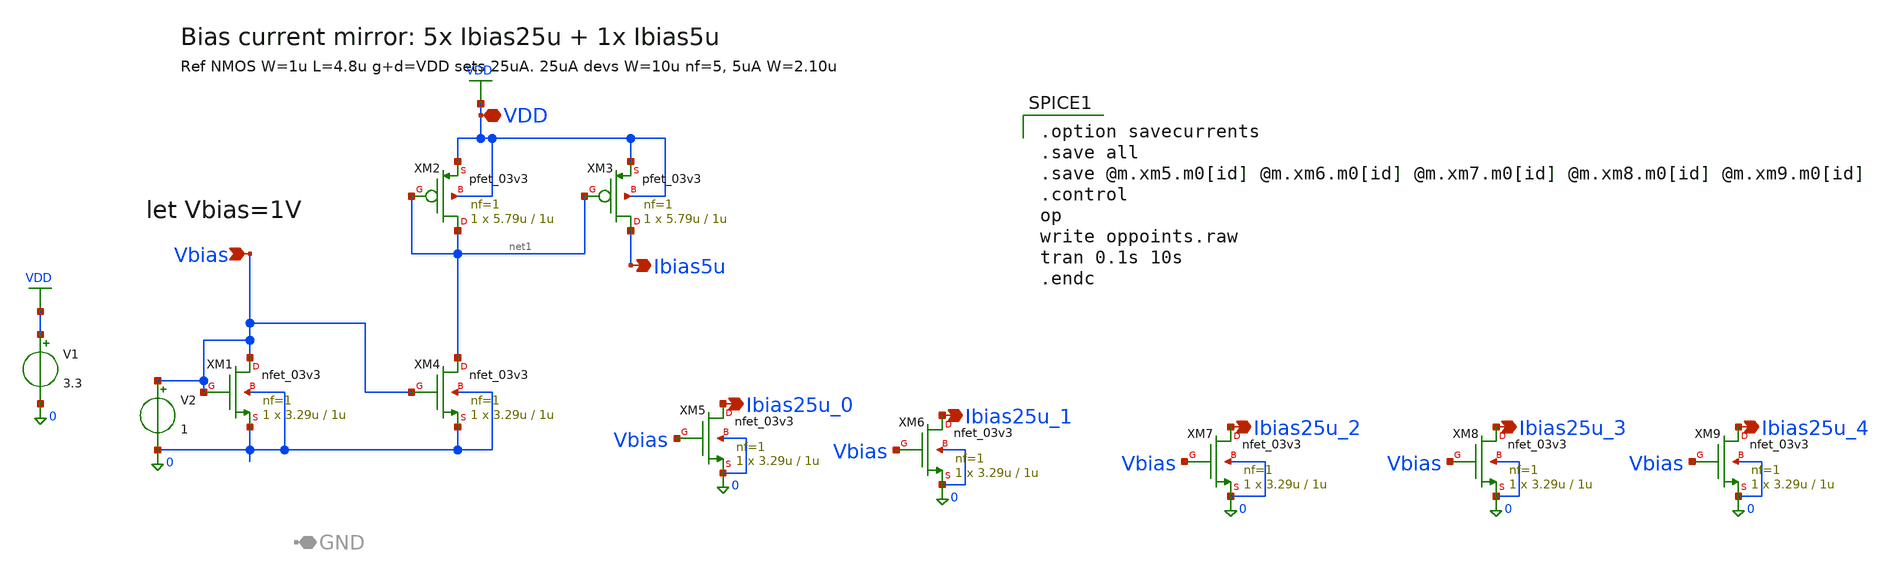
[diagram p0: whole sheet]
** sch_path: ps-bias/jz_bias_tb.sch
**.subckt jz_bias_tb Ibias25u_0 Ibias25u_1 Ibias25u_2 Ibias25u_3 Ibias25u_4 Ibias5u VDD Vbias
*.opin Ibias25u_0
*.opin Ibias25u_1
*.opin Ibias25u_2
*.opin Ibias25u_3
*.opin Ibias25u_4
*.opin Ibias5u
*.iopin VDD
*.ipin Vbias
XM2 net1 net1 VDD VDD pfet_03v3 L=1u W=5.79u nf=1 ad='int((nf+1)/2) * W/nf * 0.18u' as='int((nf+2)/2) * W/nf * 0.18u'
+ pd='2*int((nf+1)/2) * (W/nf + 0.18u)' ps='2*int((nf+2)/2) * (W/nf + 0.18u)' nrd='0.18u / W' nrs='0.18u / W'
+ sa=0 sb=0 sd=0 m=1
XM3 Ibias5u net1 VDD VDD pfet_03v3 L=1u W=5.79u nf=1 ad='int((nf+1)/2) * W/nf * 0.18u' as='int((nf+2)/2) * W/nf * 0.18u'
+ pd='2*int((nf+1)/2) * (W/nf + 0.18u)' ps='2*int((nf+2)/2) * (W/nf + 0.18u)' nrd='0.18u / W' nrs='0.18u / W'
+ sa=0 sb=0 sd=0 m=1
V1 VDD 0 3.3
V2 Vbias 0 1
XM1 Vbias Vbias 0 0 nfet_03v3 L=1u W=3.29u nf=1 ad='int((nf+1)/2) * W/nf * 0.18u' as='int((nf+2)/2) * W/nf * 0.18u'
+ pd='2*int((nf+1)/2) * (W/nf + 0.18u)' ps='2*int((nf+2)/2) * (W/nf + 0.18u)' nrd='0.18u / W' nrs='0.18u / W'
+ sa=0 sb=0 sd=0 m=1
XM4 net1 Vbias 0 0 nfet_03v3 L=1u W=3.29u nf=1 ad='int((nf+1)/2) * W/nf * 0.18u' as='int((nf+2)/2) * W/nf * 0.18u'
+ pd='2*int((nf+1)/2) * (W/nf + 0.18u)' ps='2*int((nf+2)/2) * (W/nf + 0.18u)' nrd='0.18u / W' nrs='0.18u / W'
+ sa=0 sb=0 sd=0 m=1
XM5 Ibias25u_0 Vbias 0 0 nfet_03v3 L=1u W=3.29u nf=1 ad='int((nf+1)/2) * W/nf * 0.18u' as='int((nf+2)/2) * W/nf * 0.18u'
+ pd='2*int((nf+1)/2) * (W/nf + 0.18u)' ps='2*int((nf+2)/2) * (W/nf + 0.18u)' nrd='0.18u / W' nrs='0.18u / W'
+ sa=0 sb=0 sd=0 m=1
XM6 Ibias25u_1 Vbias 0 0 nfet_03v3 L=1u W=3.29u nf=1 ad='int((nf+1)/2) * W/nf * 0.18u' as='int((nf+2)/2) * W/nf * 0.18u'
+ pd='2*int((nf+1)/2) * (W/nf + 0.18u)' ps='2*int((nf+2)/2) * (W/nf + 0.18u)' nrd='0.18u / W' nrs='0.18u / W'
+ sa=0 sb=0 sd=0 m=1
XM7 Ibias25u_2 Vbias 0 0 nfet_03v3 L=1u W=3.29u nf=1 ad='int((nf+1)/2) * W/nf * 0.18u' as='int((nf+2)/2) * W/nf * 0.18u'
+ pd='2*int((nf+1)/2) * (W/nf + 0.18u)' ps='2*int((nf+2)/2) * (W/nf + 0.18u)' nrd='0.18u / W' nrs='0.18u / W'
+ sa=0 sb=0 sd=0 m=1
XM8 Ibias25u_3 Vbias 0 0 nfet_03v3 L=1u W=3.29u nf=1 ad='int((nf+1)/2) * W/nf * 0.18u' as='int((nf+2)/2) * W/nf * 0.18u'
+ pd='2*int((nf+1)/2) * (W/nf + 0.18u)' ps='2*int((nf+2)/2) * (W/nf + 0.18u)' nrd='0.18u / W' nrs='0.18u / W'
+ sa=0 sb=0 sd=0 m=1
XM9 Ibias25u_4 Vbias 0 0 nfet_03v3 L=1u W=3.29u nf=1 ad='int((nf+1)/2) * W/nf * 0.18u' as='int((nf+2)/2) * W/nf * 0.18u'
+ pd='2*int((nf+1)/2) * (W/nf + 0.18u)' ps='2*int((nf+2)/2) * (W/nf + 0.18u)' nrd='0.18u / W' nrs='0.18u / W'
+ sa=0 sb=0 sd=0 m=1
**** begin user architecture code

.include $::180MCU_MODELS/design.ngspice
.lib $::180MCU_MODELS/sm141064.ngspice typical
.lib $::180MCU_MODELS/sm141064.ngspice res_typical
.lib $::180MCU_MODELS/sm141064.ngspice cap_mim
.lib $::180MCU_MODELS/sm141064.ngspice mimcap_typical


.option savecurrents
.save all
.save @m.xm5.m0[id] @m.xm6.m0[id] @m.xm7.m0[id] @m.xm8.m0[id] @m.xm9.m0[id]
.control
op
write oppoints.raw
tran 0.1s 10s
.endc

**** end user architecture code
**.ends
.GLOBAL VDD
.end
